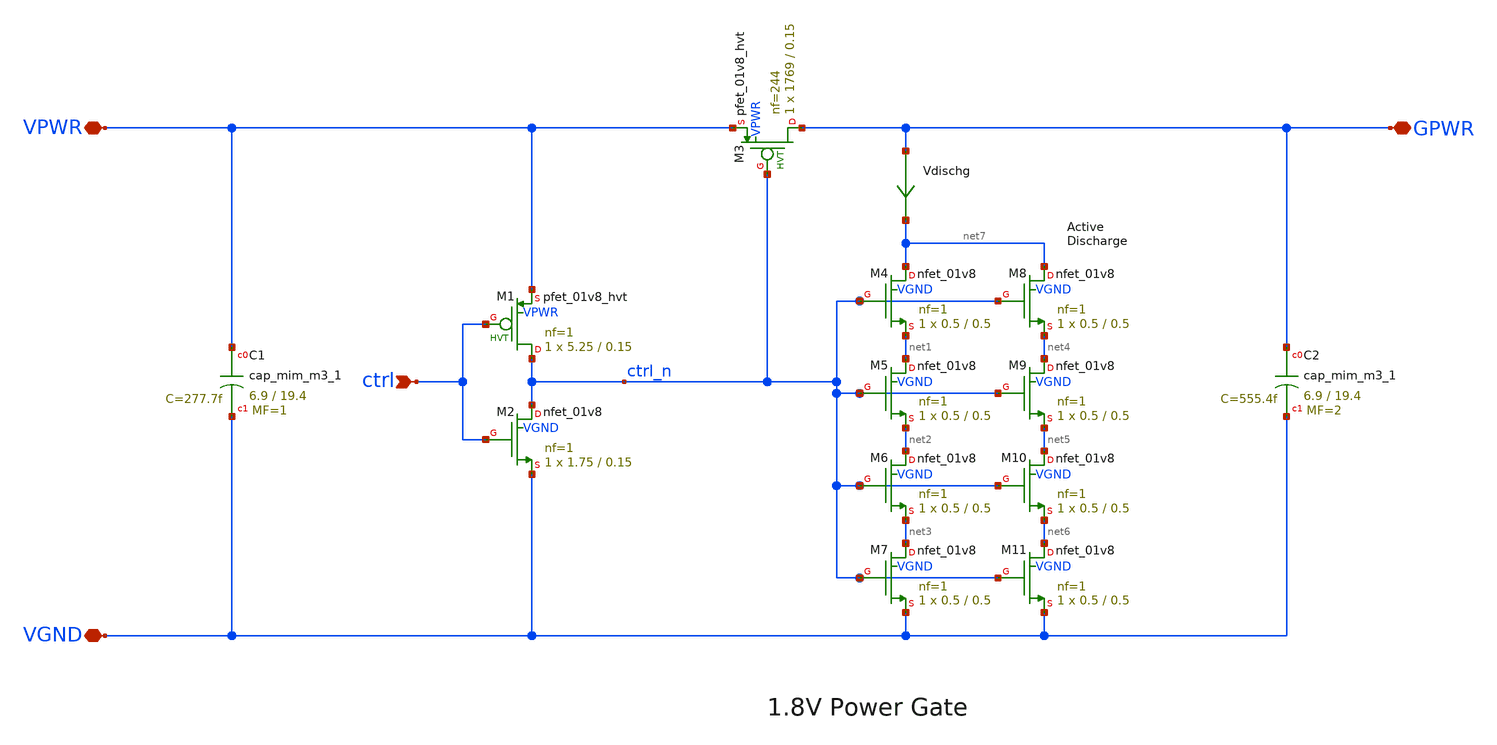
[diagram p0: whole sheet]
** sch_path: pg/sky130/tt_pg_1v8_ll_1/xschem/tt_pg_1v8_ll_1.sch
**.subckt tt_pg_1v8_ll_1 ctrl VGND VPWR GPWR
*.ipin ctrl
*.iopin VGND
*.iopin VPWR
*.iopin GPWR
XM2 ctrl_n ctrl VGND VGND sky130_fd_pr__nfet_01v8 L=0.15 W=1.75 nf=1 ad='int((nf+1)/2) * W/nf * 0.29'
+ as='int((nf+2)/2) * W/nf * 0.29' pd='2*int((nf+1)/2) * (W/nf + 0.29)' ps='2*int((nf+2)/2) * (W/nf + 0.29)'
+ nrd='0.29 / W' nrs='0.29 / W' sa=0 sb=0 sd=0 mult=1 m=1
XM1 ctrl_n ctrl VPWR VPWR sky130_fd_pr__pfet_01v8_hvt L=0.15 W=5.25 nf=1 ad='int((nf+1)/2) * W/nf * 0.29'
+ as='int((nf+2)/2) * W/nf * 0.29' pd='2*int((nf+1)/2) * (W/nf + 0.29)' ps='2*int((nf+2)/2) * (W/nf + 0.29)'
+ nrd='0.29 / W' nrs='0.29 / W' sa=0 sb=0 sd=0 mult=1 m=1
XM3 GPWR ctrl_n VPWR VPWR sky130_fd_pr__pfet_01v8_hvt L=0.15 W=1769 nf=244 ad='int((nf+1)/2) * W/nf * 0.29'
+ as='int((nf+2)/2) * W/nf * 0.29' pd='2*int((nf+1)/2) * (W/nf + 0.29)' ps='2*int((nf+2)/2) * (W/nf + 0.29)'
+ nrd='0.29 / W' nrs='0.29 / W' sa=0 sb=0 sd=0 mult=1 m=1
XM4 net7 ctrl_n net1 VGND sky130_fd_pr__nfet_01v8 L=0.5 W=0.5 nf=1 ad='int((nf+1)/2) * W/nf * 0.29' as='int((nf+2)/2) * W/nf * 0.29'
+ pd='2*int((nf+1)/2) * (W/nf + 0.29)' ps='2*int((nf+2)/2) * (W/nf + 0.29)' nrd='0.29 / W' nrs='0.29 / W'
+ sa=0 sb=0 sd=0 mult=1 m=1
Vdischg GPWR net7 0
.save i(vdischg)
XM5 net1 ctrl_n net2 VGND sky130_fd_pr__nfet_01v8 L=0.5 W=0.5 nf=1 ad='int((nf+1)/2) * W/nf * 0.29' as='int((nf+2)/2) * W/nf * 0.29'
+ pd='2*int((nf+1)/2) * (W/nf + 0.29)' ps='2*int((nf+2)/2) * (W/nf + 0.29)' nrd='0.29 / W' nrs='0.29 / W'
+ sa=0 sb=0 sd=0 mult=1 m=1
XM6 net2 ctrl_n net3 VGND sky130_fd_pr__nfet_01v8 L=0.5 W=0.5 nf=1 ad='int((nf+1)/2) * W/nf * 0.29' as='int((nf+2)/2) * W/nf * 0.29'
+ pd='2*int((nf+1)/2) * (W/nf + 0.29)' ps='2*int((nf+2)/2) * (W/nf + 0.29)' nrd='0.29 / W' nrs='0.29 / W'
+ sa=0 sb=0 sd=0 mult=1 m=1
XM7 net3 ctrl_n VGND VGND sky130_fd_pr__nfet_01v8 L=0.5 W=0.5 nf=1 ad='int((nf+1)/2) * W/nf * 0.29' as='int((nf+2)/2) * W/nf * 0.29'
+ pd='2*int((nf+1)/2) * (W/nf + 0.29)' ps='2*int((nf+2)/2) * (W/nf + 0.29)' nrd='0.29 / W' nrs='0.29 / W'
+ sa=0 sb=0 sd=0 mult=1 m=1
XM8 net7 ctrl_n net4 VGND sky130_fd_pr__nfet_01v8 L=0.5 W=0.5 nf=1 ad='int((nf+1)/2) * W/nf * 0.29' as='int((nf+2)/2) * W/nf * 0.29'
+ pd='2*int((nf+1)/2) * (W/nf + 0.29)' ps='2*int((nf+2)/2) * (W/nf + 0.29)' nrd='0.29 / W' nrs='0.29 / W'
+ sa=0 sb=0 sd=0 mult=1 m=1
XM9 net4 ctrl_n net5 VGND sky130_fd_pr__nfet_01v8 L=0.5 W=0.5 nf=1 ad='int((nf+1)/2) * W/nf * 0.29' as='int((nf+2)/2) * W/nf * 0.29'
+ pd='2*int((nf+1)/2) * (W/nf + 0.29)' ps='2*int((nf+2)/2) * (W/nf + 0.29)' nrd='0.29 / W' nrs='0.29 / W'
+ sa=0 sb=0 sd=0 mult=1 m=1
XM10 net5 ctrl_n net6 VGND sky130_fd_pr__nfet_01v8 L=0.5 W=0.5 nf=1 ad='int((nf+1)/2) * W/nf * 0.29'
+ as='int((nf+2)/2) * W/nf * 0.29' pd='2*int((nf+1)/2) * (W/nf + 0.29)' ps='2*int((nf+2)/2) * (W/nf + 0.29)'
+ nrd='0.29 / W' nrs='0.29 / W' sa=0 sb=0 sd=0 mult=1 m=1
XM11 net6 ctrl_n VGND VGND sky130_fd_pr__nfet_01v8 L=0.5 W=0.5 nf=1 ad='int((nf+1)/2) * W/nf * 0.29'
+ as='int((nf+2)/2) * W/nf * 0.29' pd='2*int((nf+1)/2) * (W/nf + 0.29)' ps='2*int((nf+2)/2) * (W/nf + 0.29)'
+ nrd='0.29 / W' nrs='0.29 / W' sa=0 sb=0 sd=0 mult=1 m=1
XC1 VPWR VGND sky130_fd_pr__cap_mim_m3_1 W=6.9 L=19.4 MF=1 m=1
XC2 GPWR VGND sky130_fd_pr__cap_mim_m3_1 W=6.9 L=19.4 MF=2 m=2
**.ends
.end
